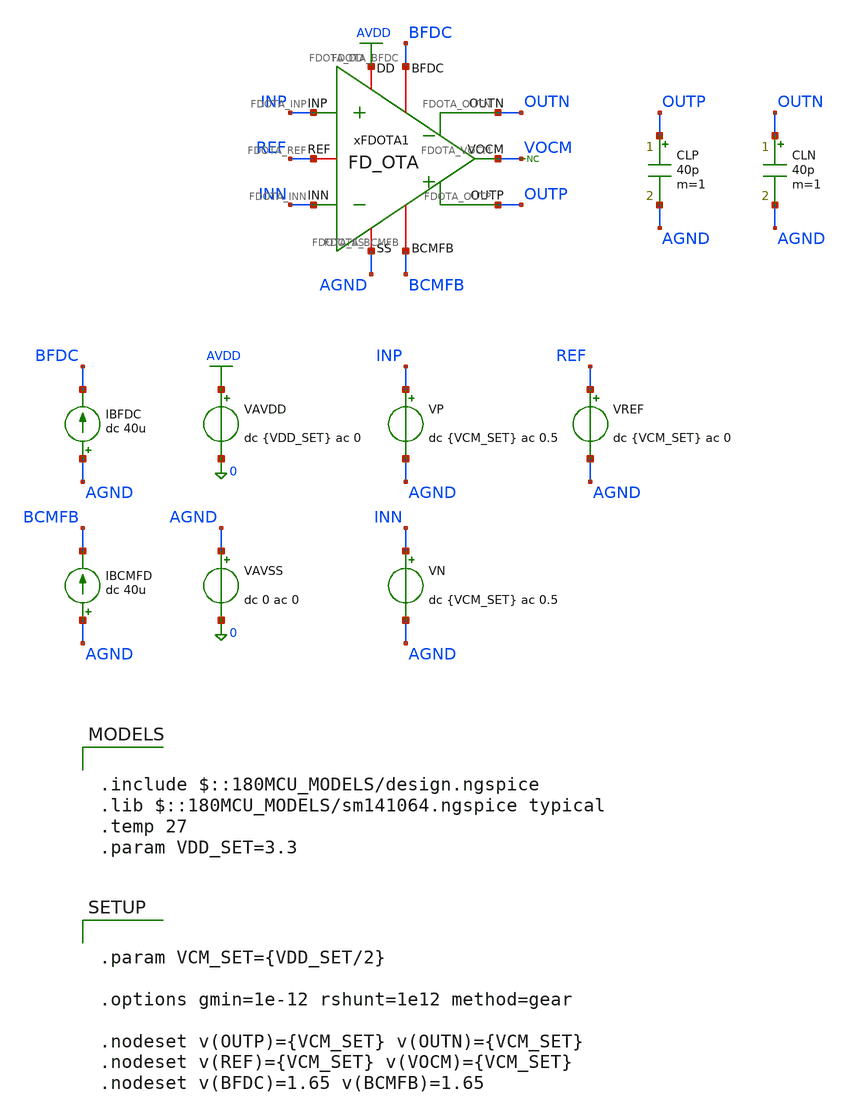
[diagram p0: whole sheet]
** sch_path: Design_Files/IC Design/Testbench/FD_OTA/FDOTA/Open_Loop/FD_OTA_TB_NOISE_NOM.sch
**.subckt FD_OTA_TB_NOISE_NOM
IBFDC AGND BFDC dc 40u
VAVDD AVDD 0 dc {VDD_SET} ac 0
.save i(vavdd)
VAVSS AGND 0 dc 0 ac 0
.save i(vavss)
VREF REF AGND dc {VCM_SET} ac 0
IBCMFD AGND BCMFB dc 40u
CLP OUTP AGND 40p m=1
CLN OUTN AGND 40p m=1
* noconn VOCM
xFDOTA1 AVDD AGND INP INN OUTN BFDC OUTP BCMFB REF VOCM FD_OTA
VP INP AGND dc {VCM_SET} ac 0.5
VN INN AGND dc {VCM_SET} ac 0.5
**** begin user architecture code

.include $::180MCU_MODELS/design.ngspice
.lib $::180MCU_MODELS/sm141064.ngspice typical
.temp 27
.param VDD_SET=3.3




.control
destroy all
save all
set wr_vecnames
set wr_singlescale
option numdgt=15

shell mkdir -p
+ /foss/designs/ECG_Acquisition_IC/Measurement_Results/IC_Simulation/FD_OTA/FDOTA/NOM.Result_txt

shell rm -f
+ /foss/designs/ECG_Acquisition_IC/Measurement_Results/IC_Simulation/FD_OTA/FDOTA/NOM.Result_txt/NOM.ol_noise_outp.txt
shell rm -f
+ /foss/designs/ECG_Acquisition_IC/Measurement_Results/IC_Simulation/FD_OTA/FDOTA/NOM.Result_txt/NOM.ol_noise_outn.txt

alter @VP[ACMAG] = 0.5
alter @VP[ACPHASE] = 0
alter @VN[ACMAG] = 0.5
alter @VN[ACPHASE] = 180
alter @VREF[ACMAG] = 0
alter @VAVDD[ACMAG] = 0
alter @VAVSS[ACMAG] = 0

op

noise v(OUTP) VP dec 100 0.01 160
setplot noise1
setscale frequency

wrdata
+ /foss/designs/ECG_Acquisition_IC/Measurement_Results/IC_Simulation/FD_OTA/FDOTA/NOM.Result_txt/NOM.ol_noise_outp.txt onoise_spectrum

reset
save all
set wr_vecnames
set wr_singlescale
option numdgt=15

alter @VP[ACMAG] = 0.5
alter @VP[ACPHASE] = 0
alter @VN[ACMAG] = 0.5
alter @VN[ACPHASE] = 180
alter @VREF[ACMAG] = 0
alter @VAVDD[ACMAG] = 0
alter @VAVSS[ACMAG] = 0

op

noise v(OUTN) VP dec 100 0.01 160
setplot noise1
setscale frequency

wrdata
+ /foss/designs/ECG_Acquisition_IC/Measurement_Results/IC_Simulation/FD_OTA/FDOTA/NOM.Result_txt/NOM.ol_noise_outn.txt onoise_spectrum

quit
.endc




.param VCM_SET={VDD_SET/2}

.options gmin=1e-12 rshunt=1e12 method=gear

.nodeset v(OUTP)={VCM_SET} v(OUTN)={VCM_SET}
.nodeset v(REF)={VCM_SET} v(VOCM)={VCM_SET}
.nodeset v(BFDC)=1.65 v(BCMFB)=1.65


**** end user architecture code
**.ends

* expanding   symbol:  ECG_Acquisition_IC/Design_Files/IC Design/Schematic/FD_OTA/FDOTA/FD_OTA.sym #
*+ of pins=10
** sym_path: Design_Files/IC Design/Schematic/FD_OTA/FDOTA/FD_OTA.sym
** sch_path: Design_Files/IC Design/Schematic/FD_OTA/FDOTA/FD_OTA.sch
.subckt FD_OTA FDOTA_DD FDOTA_SS FDOTA_INP FDOTA_INN FDOTA_OUTN FDOTA_BFDC FDOTA_OUTP FDOTA_BCMFB
+ FDOTA_REF FDOTA_VOCM
*.iopin FDOTA_DD
*.iopin FDOTA_SS
*.ipin FDOTA_INP
*.ipin FDOTA_INN
*.opin FDOTA_OUTP
*.iopin FDOTA_BFDC
*.opin FDOTA_OUTN
*.iopin FDOTA_BCMFB
*.iopin FDOTA_REF
*.iopin FDOTA_VOCM
R1 FDOTA_OUTP FDOTA_VOCM 100k m=1
R2 FDOTA_VOCM FDOTA_OUTN 100k m=1
C1 FDOTA_OUTP FDOTA_VOCM 50f m=1
C2 FDOTA_VOCM FDOTA_OUTN 50f m=1
xFDC1 FDOTA_DD FDOTA_SS FDOTA_INP FDOTA_INN FDOTA_OUTN FDOTA_BFDC FDOTA_OUTP FDOTA_VCMFB FDC
xCMFB1 FDOTA_DD FDOTA_SS FDOTA_VOCM FDOTA_REF FDOTA_VCMFB FDOTA_BCMFB CMFB
.ends


* expanding   symbol:  ECG_Acquisition_IC/Design_Files/IC Design/Schematic/FD_OTA/FDC/FDC.sym # of
*+ pins=8
** sym_path: Design_Files/IC Design/Schematic/FD_OTA/FDC/FDC.sym
** sch_path: Design_Files/IC Design/Schematic/FD_OTA/FDC/FDC.sch
.subckt FDC FDC_DD FDC_SS FDC_INP FDC_INN FDC_OUTN FDC_B FDC_OUTP FDC_CMFB
*.iopin FDC_DD
*.iopin FDC_SS
*.ipin FDC_INP
*.ipin FDC_INN
*.opin FDC_OUTP
*.iopin FDC_B
*.opin FDC_OUTN
*.iopin FDC_CMFB
XM3 net4 FDC_CMFB FDC_DD FDC_DD pfet_03v3 L=2u W=1u nf=1 ad='int((nf+1)/2) * W/nf * 0.18u' as='int((nf+2)/2) * W/nf * 0.18u'
+ pd='2*int((nf+1)/2) * (W/nf + 0.18u)' ps='2*int((nf+2)/2) * (W/nf + 0.18u)' nrd='0.18u / W' nrs='0.18u / W'
+ sa=0 sb=0 sd=0 m=200
XM8 FDC_OUTP FDC_B FDC_SS FDC_SS nfet_03v3 L=0.5u W=1u nf=1 ad='int((nf+1)/2) * W/nf * 0.18u' as='int((nf+2)/2) * W/nf * 0.18u'
+ pd='2*int((nf+1)/2) * (W/nf + 0.18u)' ps='2*int((nf+2)/2) * (W/nf + 0.18u)' nrd='0.18u / W' nrs='0.18u / W'
+ sa=0 sb=0 sd=0 m=100
Rz net1 net2 3.5k m=1
XM5 net3 FDC_B FDC_SS FDC_SS nfet_03v3 L=2u W=1u nf=1 ad='int((nf+1)/2) * W/nf * 0.18u' as='int((nf+2)/2) * W/nf * 0.18u'
+ pd='2*int((nf+1)/2) * (W/nf + 0.18u)' ps='2*int((nf+2)/2) * (W/nf + 0.18u)' nrd='0.18u / W' nrs='0.18u / W'
+ sa=0 sb=0 sd=0 m=10
XM6 FDC_OUTP net1 FDC_DD FDC_DD pfet_03v3 L=0.5u W=1u nf=1 ad='int((nf+1)/2) * W/nf * 0.18u' as='int((nf+2)/2) * W/nf * 0.18u'
+ pd='2*int((nf+1)/2) * (W/nf + 0.18u)' ps='2*int((nf+2)/2) * (W/nf + 0.18u)' nrd='0.18u / W' nrs='0.18u / W'
+ sa=0 sb=0 sd=0 m=200
XM10 FDC_B FDC_B FDC_SS FDC_SS nfet_03v3 L=2u W=1u nf=1 ad='int((nf+1)/2) * W/nf * 0.18u' as='int((nf+2)/2) * W/nf * 0.18u'
+ pd='2*int((nf+1)/2) * (W/nf + 0.18u)' ps='2*int((nf+2)/2) * (W/nf + 0.18u)' nrd='0.18u / W' nrs='0.18u / W'
+ sa=0 sb=0 sd=0 m=20
Cc net2 FDC_OUTP 2.5p m=1
XM9 FDC_OUTN FDC_B FDC_SS FDC_SS nfet_03v3 L=0.5u W=1u nf=1 ad='int((nf+1)/2) * W/nf * 0.18u' as='int((nf+2)/2) * W/nf * 0.18u'
+ pd='2*int((nf+1)/2) * (W/nf + 0.18u)' ps='2*int((nf+2)/2) * (W/nf + 0.18u)' nrd='0.18u / W' nrs='0.18u / W'
+ sa=0 sb=0 sd=0 m=100
Rz1 net4 net5 3.5k m=1
XM7 FDC_OUTN net4 FDC_DD FDC_DD pfet_03v3 L=0.5u W=1u nf=1 ad='int((nf+1)/2) * W/nf * 0.18u' as='int((nf+2)/2) * W/nf * 0.18u'
+ pd='2*int((nf+1)/2) * (W/nf + 0.18u)' ps='2*int((nf+2)/2) * (W/nf + 0.18u)' nrd='0.18u / W' nrs='0.18u / W'
+ sa=0 sb=0 sd=0 m=200
Cc1 net5 FDC_OUTN 2.5p m=1
XM4 net1 FDC_CMFB FDC_DD FDC_DD pfet_03v3 L=2u W=1u nf=1 ad='int((nf+1)/2) * W/nf * 0.18u' as='int((nf+2)/2) * W/nf * 0.18u'
+ pd='2*int((nf+1)/2) * (W/nf + 0.18u)' ps='2*int((nf+2)/2) * (W/nf + 0.18u)' nrd='0.18u / W' nrs='0.18u / W'
+ sa=0 sb=0 sd=0 m=200
XM1 net4 FDC_INN net3 FDC_SS nfet_03v3 L=2u W=1u nf=1 ad='int((nf+1)/2) * W/nf * 0.18u' as='int((nf+2)/2) * W/nf * 0.18u'
+ pd='2*int((nf+1)/2) * (W/nf + 0.18u)' ps='2*int((nf+2)/2) * (W/nf + 0.18u)' nrd='0.18u / W' nrs='0.18u / W'
+ sa=0 sb=0 sd=0 m=200
XM2 net1 FDC_INP net3 FDC_SS nfet_03v3 L=2u W=1u nf=1 ad='int((nf+1)/2) * W/nf * 0.18u' as='int((nf+2)/2) * W/nf * 0.18u'
+ pd='2*int((nf+1)/2) * (W/nf + 0.18u)' ps='2*int((nf+2)/2) * (W/nf + 0.18u)' nrd='0.18u / W' nrs='0.18u / W'
+ sa=0 sb=0 sd=0 m=200
.ends


* expanding   symbol:  ECG_Acquisition_IC/Design_Files/IC Design/Schematic/FD_OTA/CMFB/CMFB.sym # of
*+ pins=6
** sym_path: Design_Files/IC Design/Schematic/FD_OTA/CMFB/CMFB.sym
** sch_path: Design_Files/IC Design/Schematic/FD_OTA/CMFB/CMFB.sch
.subckt CMFB CMFB_DD CMFB_SS CMFB_IN CMFB_REF CMFB_OUT CMFB_B
*.iopin CMFB_DD
*.iopin CMFB_SS
*.ipin CMFB_IN
*.ipin CMFB_REF
*.opin CMFB_OUT
*.iopin CMFB_B
XM4 CMFB_OUT CMFB_OUT CMFB_DD CMFB_DD pfet_03v3 L=0.5u W=1u nf=1 ad='int((nf+1)/2) * W/nf * 0.18u' as='int((nf+2)/2) * W/nf * 0.18u'
+ pd='2*int((nf+1)/2) * (W/nf + 0.18u)' ps='2*int((nf+2)/2) * (W/nf + 0.18u)' nrd='0.18u / W' nrs='0.18u / W'
+ sa=0 sb=0 sd=0 m=77
XM3 net2 net2 CMFB_DD CMFB_DD pfet_03v3 L=0.5u W=1u nf=1 ad='int((nf+1)/2) * W/nf * 0.18u' as='int((nf+2)/2) * W/nf * 0.18u'
+ pd='2*int((nf+1)/2) * (W/nf + 0.18u)' ps='2*int((nf+2)/2) * (W/nf + 0.18u)' nrd='0.18u / W' nrs='0.18u / W'
+ sa=0 sb=0 sd=0 m=77
XM1 net2 CMFB_REF net1 CMFB_SS nfet_03v3 L=0.5u W=1u nf=1 ad='int((nf+1)/2) * W/nf * 0.18u' as='int((nf+2)/2) * W/nf * 0.18u'
+ pd='2*int((nf+1)/2) * (W/nf + 0.18u)' ps='2*int((nf+2)/2) * (W/nf + 0.18u)' nrd='0.18u / W' nrs='0.18u / W'
+ sa=0 sb=0 sd=0 m=5
XM2 CMFB_OUT CMFB_IN net1 CMFB_SS nfet_03v3 L=0.5u W=1u nf=1 ad='int((nf+1)/2) * W/nf * 0.18u' as='int((nf+2)/2) * W/nf * 0.18u'
+ pd='2*int((nf+1)/2) * (W/nf + 0.18u)' ps='2*int((nf+2)/2) * (W/nf + 0.18u)' nrd='0.18u / W' nrs='0.18u / W'
+ sa=0 sb=0 sd=0 m=5
XM5 net1 CMFB_B CMFB_SS CMFB_SS nfet_03v3 L=2u W=1u nf=1 ad='int((nf+1)/2) * W/nf * 0.18u' as='int((nf+2)/2) * W/nf * 0.18u'
+ pd='2*int((nf+1)/2) * (W/nf + 0.18u)' ps='2*int((nf+2)/2) * (W/nf + 0.18u)' nrd='0.18u / W' nrs='0.18u / W'
+ sa=0 sb=0 sd=0 m=20
XM10 CMFB_B CMFB_B CMFB_SS CMFB_SS nfet_03v3 L=2u W=1u nf=1 ad='int((nf+1)/2) * W/nf * 0.18u' as='int((nf+2)/2) * W/nf * 0.18u'
+ pd='2*int((nf+1)/2) * (W/nf + 0.18u)' ps='2*int((nf+2)/2) * (W/nf + 0.18u)' nrd='0.18u / W' nrs='0.18u / W'
+ sa=0 sb=0 sd=0 m=20
.ends

.GLOBAL AVDD
.end
